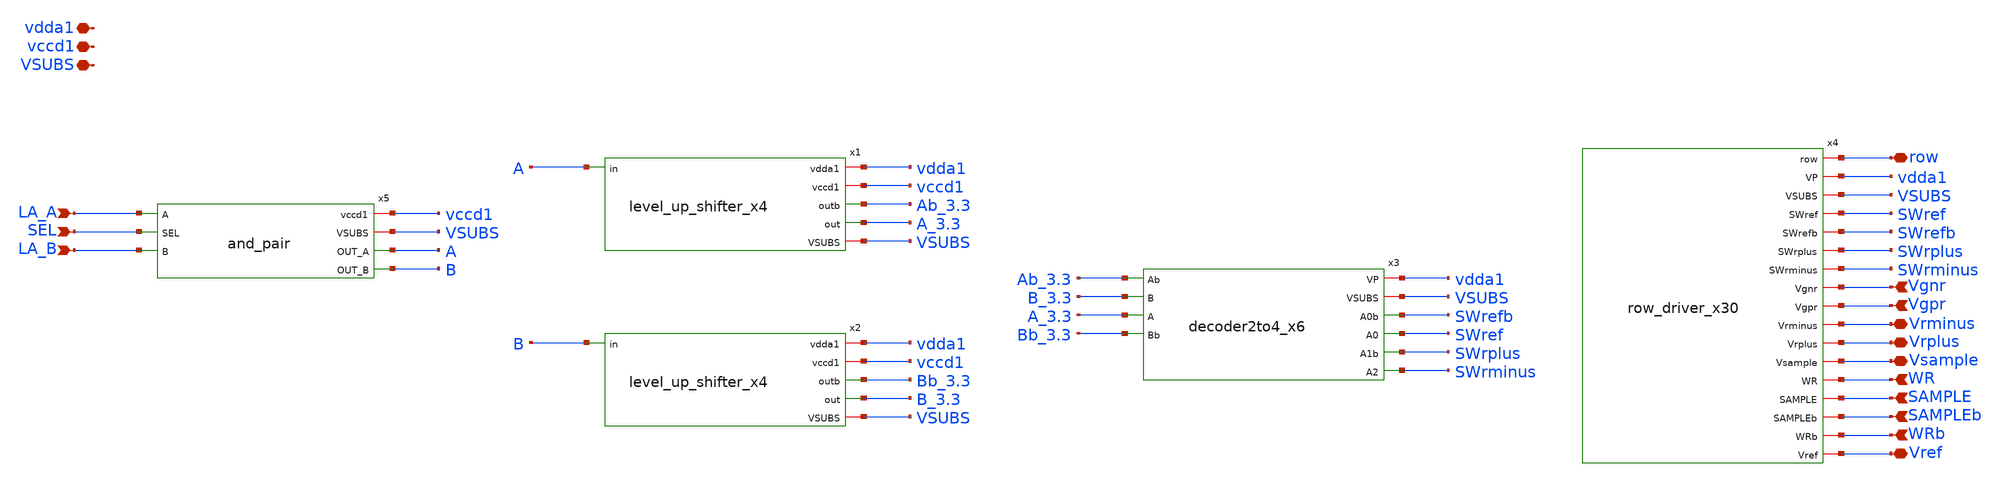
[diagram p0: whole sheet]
** sch_path: xschem/row_driver_big.sch
**.subckt row_driver_big vccd1 vdda1 VSUBS LA_A LA_B row Vref Vrplus Vrminus Vgpr Vgnr Vsample WR
*+ SAMPLE SAMPLEb WRb SEL
*.iopin vccd1
*.iopin vdda1
*.iopin VSUBS
*.ipin LA_A
*.ipin LA_B
*.iopin row
*.iopin Vref
*.iopin Vrplus
*.iopin Vrminus
*.ipin Vgpr
*.ipin Vgnr
*.iopin Vsample
*.ipin WR
*.ipin SAMPLE
*.ipin SAMPLEb
*.ipin WRb
*.ipin SEL
x1 vdda1 vccd1 A Ab_3.3 A_3.3 VSUBS level_up_shifter_x4
x2 vdda1 vccd1 B Bb_3.3 B_3.3 VSUBS level_up_shifter_x4
x3 vdda1 VSUBS Ab_3.3 SWrefb B_3.3 SWref SWrplus A_3.3 Bb_3.3 SWrminus decoder2to4_x6
x4 row vdda1 VSUBS SWref SWrefb SWrplus SWrminus Vgnr Vgpr Vrminus Vrplus Vsample WR SAMPLE SAMPLEb
+ WRb Vref row_driver_x30
x5 vccd1 VSUBS LA_A SEL A LA_B B and_pair
**.ends
.end
